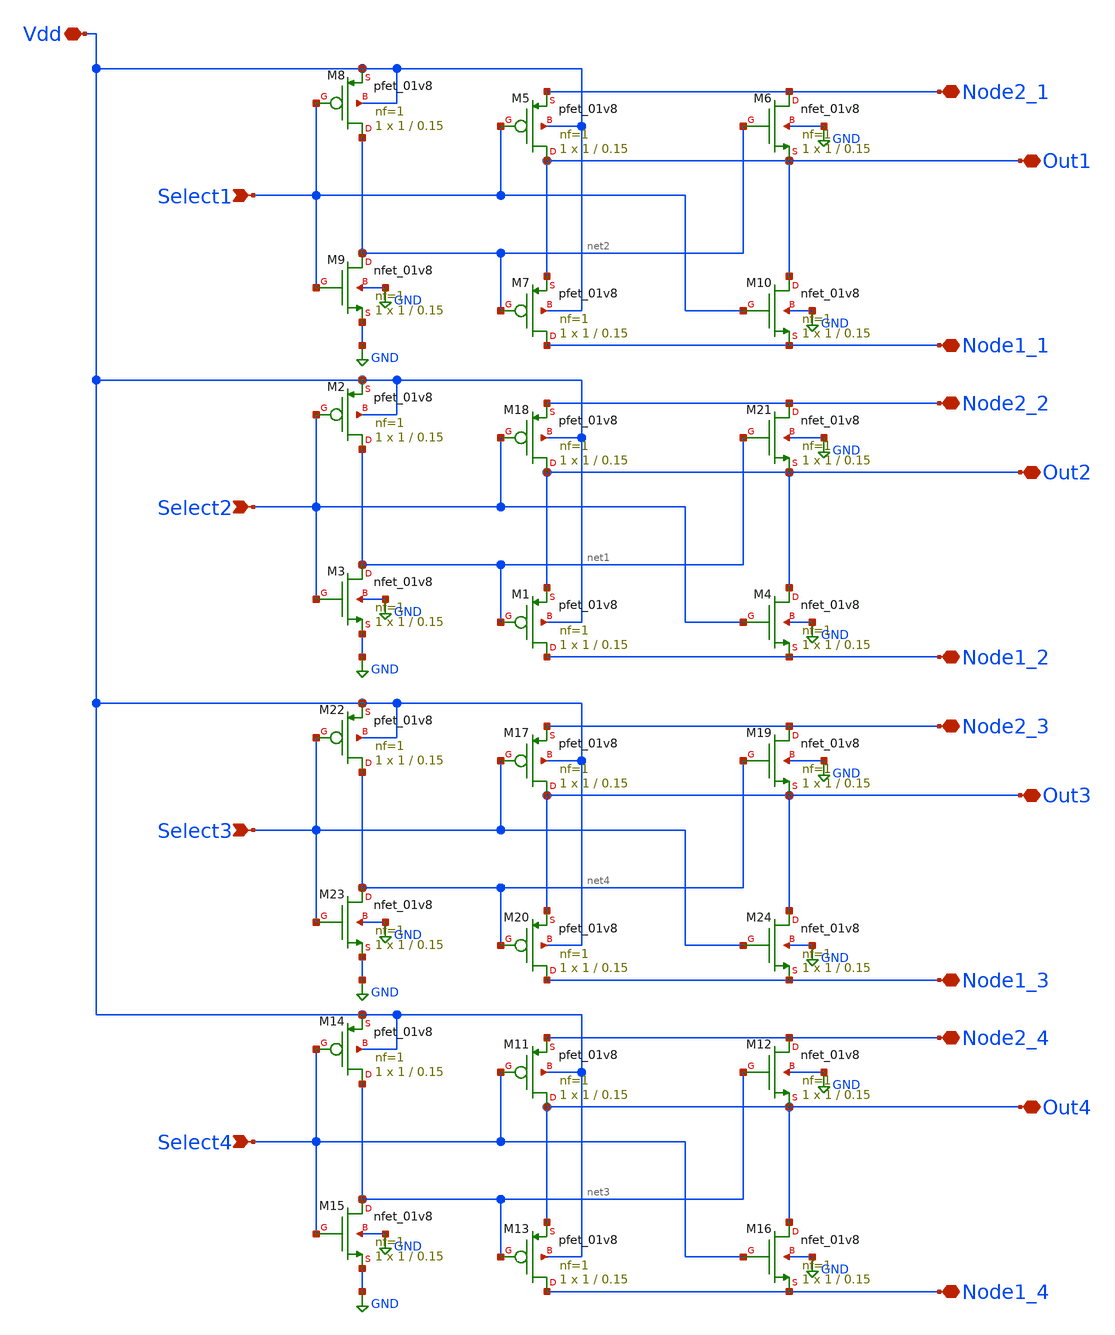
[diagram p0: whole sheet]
** sch_path: libs.ref/sky130_hilas_sc/xschem/Tgate4Double01.sch
**.subckt Tgate4Double01 Select2 Vdd Node1_2 Out2 Node2_2 Select1 Node1_1 Out1 Node2_1 Select4
*+ Node1_4 Out4 Node2_4 Select3 Node1_3 Out3 Node2_3
*.ipin Select2
*.iopin Vdd
*.iopin Node1_2
*.iopin Out2
*.iopin Node2_2
*.ipin Select1
*.iopin Node1_1
*.iopin Out1
*.iopin Node2_1
*.ipin Select4
*.iopin Node1_4
*.iopin Out4
*.iopin Node2_4
*.ipin Select3
*.iopin Node1_3
*.iopin Out3
*.iopin Node2_3
XM18 Out2 Select2 Node2_2 Vdd sky130_fd_pr__pfet_01v8 L=0.15 W=1 nf=1 ad='int((nf+1)/2) * W/nf * 0.29'
+ as='int((nf+2)/2) * W/nf * 0.29' pd='2*int((nf+1)/2) * (W/nf + 0.29)' ps='2*int((nf+2)/2) * (W/nf + 0.29)'
+ nrd='0.29 / W' nrs='0.29 / W' sa=0 sb=0 sd=0 mult=1 m=1
XM21 Node2_2 net1 Out2 GND sky130_fd_pr__nfet_01v8 L=0.15 W=1 nf=1 ad='int((nf+1)/2) * W/nf * 0.29' as='int((nf+2)/2) * W/nf * 0.29'
+ pd='2*int((nf+1)/2) * (W/nf + 0.29)' ps='2*int((nf+2)/2) * (W/nf + 0.29)' nrd='0.29 / W' nrs='0.29 / W'
+ sa=0 sb=0 sd=0 mult=1 m=1
XM1 Node1_2 net1 Out2 Vdd sky130_fd_pr__pfet_01v8 L=0.15 W=1 nf=1 ad='int((nf+1)/2) * W/nf * 0.29' as='int((nf+2)/2) * W/nf * 0.29'
+ pd='2*int((nf+1)/2) * (W/nf + 0.29)' ps='2*int((nf+2)/2) * (W/nf + 0.29)' nrd='0.29 / W' nrs='0.29 / W'
+ sa=0 sb=0 sd=0 mult=1 m=1
XM2 net1 Select2 Vdd Vdd sky130_fd_pr__pfet_01v8 L=0.15 W=1 nf=1 ad='int((nf+1)/2) * W/nf * 0.29' as='int((nf+2)/2) * W/nf * 0.29'
+ pd='2*int((nf+1)/2) * (W/nf + 0.29)' ps='2*int((nf+2)/2) * (W/nf + 0.29)' nrd='0.29 / W' nrs='0.29 / W'
+ sa=0 sb=0 sd=0 mult=1 m=1
XM3 net1 Select2 GND GND sky130_fd_pr__nfet_01v8 L=0.15 W=1 nf=1 ad='int((nf+1)/2) * W/nf * 0.29' as='int((nf+2)/2) * W/nf * 0.29'
+ pd='2*int((nf+1)/2) * (W/nf + 0.29)' ps='2*int((nf+2)/2) * (W/nf + 0.29)' nrd='0.29 / W' nrs='0.29 / W'
+ sa=0 sb=0 sd=0 mult=1 m=1
XM4 Out2 Select2 Node1_2 GND sky130_fd_pr__nfet_01v8 L=0.15 W=1 nf=1 ad='int((nf+1)/2) * W/nf * 0.29'
+ as='int((nf+2)/2) * W/nf * 0.29' pd='2*int((nf+1)/2) * (W/nf + 0.29)' ps='2*int((nf+2)/2) * (W/nf + 0.29)'
+ nrd='0.29 / W' nrs='0.29 / W' sa=0 sb=0 sd=0 mult=1 m=1
XM5 Out1 Select1 Node2_1 Vdd sky130_fd_pr__pfet_01v8 L=0.15 W=1 nf=1 ad='int((nf+1)/2) * W/nf * 0.29'
+ as='int((nf+2)/2) * W/nf * 0.29' pd='2*int((nf+1)/2) * (W/nf + 0.29)' ps='2*int((nf+2)/2) * (W/nf + 0.29)'
+ nrd='0.29 / W' nrs='0.29 / W' sa=0 sb=0 sd=0 mult=1 m=1
XM6 Node2_1 net2 Out1 GND sky130_fd_pr__nfet_01v8 L=0.15 W=1 nf=1 ad='int((nf+1)/2) * W/nf * 0.29' as='int((nf+2)/2) * W/nf * 0.29'
+ pd='2*int((nf+1)/2) * (W/nf + 0.29)' ps='2*int((nf+2)/2) * (W/nf + 0.29)' nrd='0.29 / W' nrs='0.29 / W'
+ sa=0 sb=0 sd=0 mult=1 m=1
XM7 Node1_1 net2 Out1 Vdd sky130_fd_pr__pfet_01v8 L=0.15 W=1 nf=1 ad='int((nf+1)/2) * W/nf * 0.29' as='int((nf+2)/2) * W/nf * 0.29'
+ pd='2*int((nf+1)/2) * (W/nf + 0.29)' ps='2*int((nf+2)/2) * (W/nf + 0.29)' nrd='0.29 / W' nrs='0.29 / W'
+ sa=0 sb=0 sd=0 mult=1 m=1
XM8 net2 Select1 Vdd Vdd sky130_fd_pr__pfet_01v8 L=0.15 W=1 nf=1 ad='int((nf+1)/2) * W/nf * 0.29' as='int((nf+2)/2) * W/nf * 0.29'
+ pd='2*int((nf+1)/2) * (W/nf + 0.29)' ps='2*int((nf+2)/2) * (W/nf + 0.29)' nrd='0.29 / W' nrs='0.29 / W'
+ sa=0 sb=0 sd=0 mult=1 m=1
XM9 net2 Select1 GND GND sky130_fd_pr__nfet_01v8 L=0.15 W=1 nf=1 ad='int((nf+1)/2) * W/nf * 0.29' as='int((nf+2)/2) * W/nf * 0.29'
+ pd='2*int((nf+1)/2) * (W/nf + 0.29)' ps='2*int((nf+2)/2) * (W/nf + 0.29)' nrd='0.29 / W' nrs='0.29 / W'
+ sa=0 sb=0 sd=0 mult=1 m=1
XM10 Out1 Select1 Node1_1 GND sky130_fd_pr__nfet_01v8 L=0.15 W=1 nf=1 ad='int((nf+1)/2) * W/nf * 0.29'
+ as='int((nf+2)/2) * W/nf * 0.29' pd='2*int((nf+1)/2) * (W/nf + 0.29)' ps='2*int((nf+2)/2) * (W/nf + 0.29)'
+ nrd='0.29 / W' nrs='0.29 / W' sa=0 sb=0 sd=0 mult=1 m=1
XM11 Out4 Select4 Node2_4 Vdd sky130_fd_pr__pfet_01v8 L=0.15 W=1 nf=1 ad='int((nf+1)/2) * W/nf * 0.29'
+ as='int((nf+2)/2) * W/nf * 0.29' pd='2*int((nf+1)/2) * (W/nf + 0.29)' ps='2*int((nf+2)/2) * (W/nf + 0.29)'
+ nrd='0.29 / W' nrs='0.29 / W' sa=0 sb=0 sd=0 mult=1 m=1
XM12 Node2_4 net3 Out4 GND sky130_fd_pr__nfet_01v8 L=0.15 W=1 nf=1 ad='int((nf+1)/2) * W/nf * 0.29' as='int((nf+2)/2) * W/nf * 0.29'
+ pd='2*int((nf+1)/2) * (W/nf + 0.29)' ps='2*int((nf+2)/2) * (W/nf + 0.29)' nrd='0.29 / W' nrs='0.29 / W'
+ sa=0 sb=0 sd=0 mult=1 m=1
XM13 Node1_4 net3 Out4 Vdd sky130_fd_pr__pfet_01v8 L=0.15 W=1 nf=1 ad='int((nf+1)/2) * W/nf * 0.29' as='int((nf+2)/2) * W/nf * 0.29'
+ pd='2*int((nf+1)/2) * (W/nf + 0.29)' ps='2*int((nf+2)/2) * (W/nf + 0.29)' nrd='0.29 / W' nrs='0.29 / W'
+ sa=0 sb=0 sd=0 mult=1 m=1
XM14 net3 Select4 Vdd Vdd sky130_fd_pr__pfet_01v8 L=0.15 W=1 nf=1 ad='int((nf+1)/2) * W/nf * 0.29' as='int((nf+2)/2) * W/nf * 0.29'
+ pd='2*int((nf+1)/2) * (W/nf + 0.29)' ps='2*int((nf+2)/2) * (W/nf + 0.29)' nrd='0.29 / W' nrs='0.29 / W'
+ sa=0 sb=0 sd=0 mult=1 m=1
XM15 net3 Select4 GND GND sky130_fd_pr__nfet_01v8 L=0.15 W=1 nf=1 ad='int((nf+1)/2) * W/nf * 0.29' as='int((nf+2)/2) * W/nf * 0.29'
+ pd='2*int((nf+1)/2) * (W/nf + 0.29)' ps='2*int((nf+2)/2) * (W/nf + 0.29)' nrd='0.29 / W' nrs='0.29 / W'
+ sa=0 sb=0 sd=0 mult=1 m=1
XM16 Out4 Select4 Node1_4 GND sky130_fd_pr__nfet_01v8 L=0.15 W=1 nf=1 ad='int((nf+1)/2) * W/nf * 0.29'
+ as='int((nf+2)/2) * W/nf * 0.29' pd='2*int((nf+1)/2) * (W/nf + 0.29)' ps='2*int((nf+2)/2) * (W/nf + 0.29)'
+ nrd='0.29 / W' nrs='0.29 / W' sa=0 sb=0 sd=0 mult=1 m=1
XM17 Out3 Select3 Node2_3 Vdd sky130_fd_pr__pfet_01v8 L=0.15 W=1 nf=1 ad='int((nf+1)/2) * W/nf * 0.29'
+ as='int((nf+2)/2) * W/nf * 0.29' pd='2*int((nf+1)/2) * (W/nf + 0.29)' ps='2*int((nf+2)/2) * (W/nf + 0.29)'
+ nrd='0.29 / W' nrs='0.29 / W' sa=0 sb=0 sd=0 mult=1 m=1
XM19 Node2_3 net4 Out3 GND sky130_fd_pr__nfet_01v8 L=0.15 W=1 nf=1 ad='int((nf+1)/2) * W/nf * 0.29' as='int((nf+2)/2) * W/nf * 0.29'
+ pd='2*int((nf+1)/2) * (W/nf + 0.29)' ps='2*int((nf+2)/2) * (W/nf + 0.29)' nrd='0.29 / W' nrs='0.29 / W'
+ sa=0 sb=0 sd=0 mult=1 m=1
XM20 Node1_3 net4 Out3 Vdd sky130_fd_pr__pfet_01v8 L=0.15 W=1 nf=1 ad='int((nf+1)/2) * W/nf * 0.29' as='int((nf+2)/2) * W/nf * 0.29'
+ pd='2*int((nf+1)/2) * (W/nf + 0.29)' ps='2*int((nf+2)/2) * (W/nf + 0.29)' nrd='0.29 / W' nrs='0.29 / W'
+ sa=0 sb=0 sd=0 mult=1 m=1
XM22 net4 Select3 Vdd Vdd sky130_fd_pr__pfet_01v8 L=0.15 W=1 nf=1 ad='int((nf+1)/2) * W/nf * 0.29' as='int((nf+2)/2) * W/nf * 0.29'
+ pd='2*int((nf+1)/2) * (W/nf + 0.29)' ps='2*int((nf+2)/2) * (W/nf + 0.29)' nrd='0.29 / W' nrs='0.29 / W'
+ sa=0 sb=0 sd=0 mult=1 m=1
XM23 net4 Select3 GND GND sky130_fd_pr__nfet_01v8 L=0.15 W=1 nf=1 ad='int((nf+1)/2) * W/nf * 0.29' as='int((nf+2)/2) * W/nf * 0.29'
+ pd='2*int((nf+1)/2) * (W/nf + 0.29)' ps='2*int((nf+2)/2) * (W/nf + 0.29)' nrd='0.29 / W' nrs='0.29 / W'
+ sa=0 sb=0 sd=0 mult=1 m=1
XM24 Out3 Select3 Node1_3 GND sky130_fd_pr__nfet_01v8 L=0.15 W=1 nf=1 ad='int((nf+1)/2) * W/nf * 0.29'
+ as='int((nf+2)/2) * W/nf * 0.29' pd='2*int((nf+1)/2) * (W/nf + 0.29)' ps='2*int((nf+2)/2) * (W/nf + 0.29)'
+ nrd='0.29 / W' nrs='0.29 / W' sa=0 sb=0 sd=0 mult=1 m=1
**.ends
.GLOBAL GND
.end
